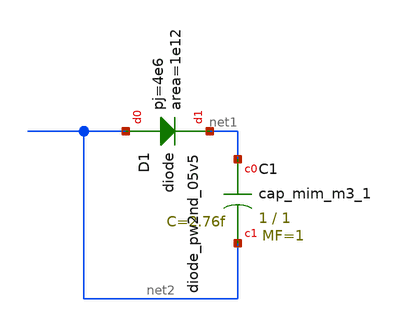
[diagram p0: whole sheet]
** sch_path: Neuron/voltContrOsc/sch/currInt.sch
**.subckt currInt
XC1 net1 net2 sky130_fd_pr__cap_mim_m3_1 W=1 L=1 MF=1 m=1
XD1 net2 net1 sky130_fd_pr__diode_pw2nd_05v5 area=1e12 pj=4e6
**.ends
.end
